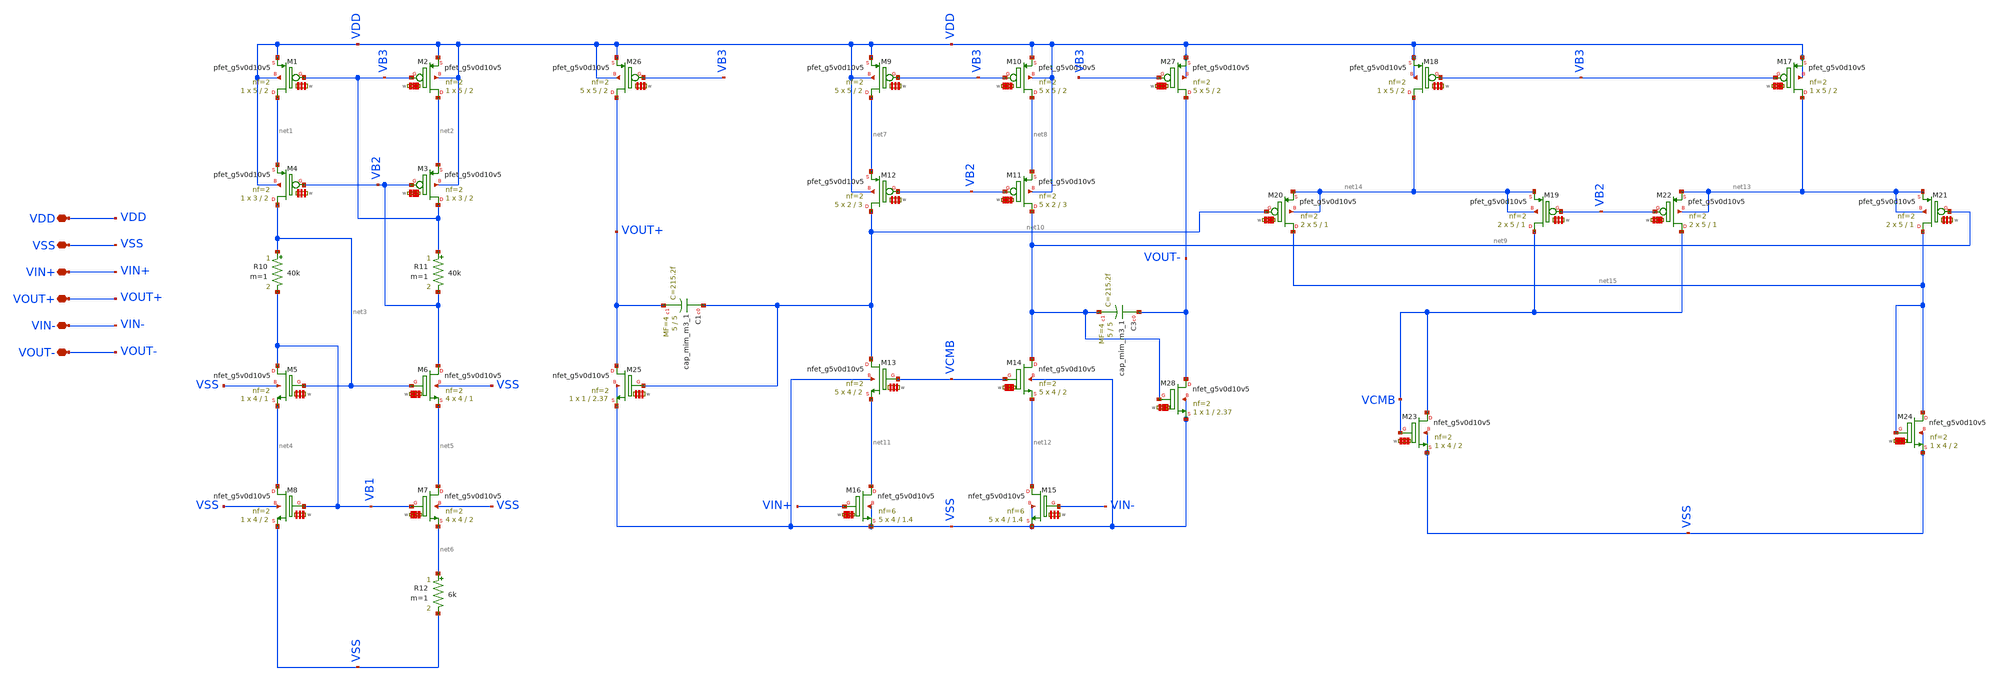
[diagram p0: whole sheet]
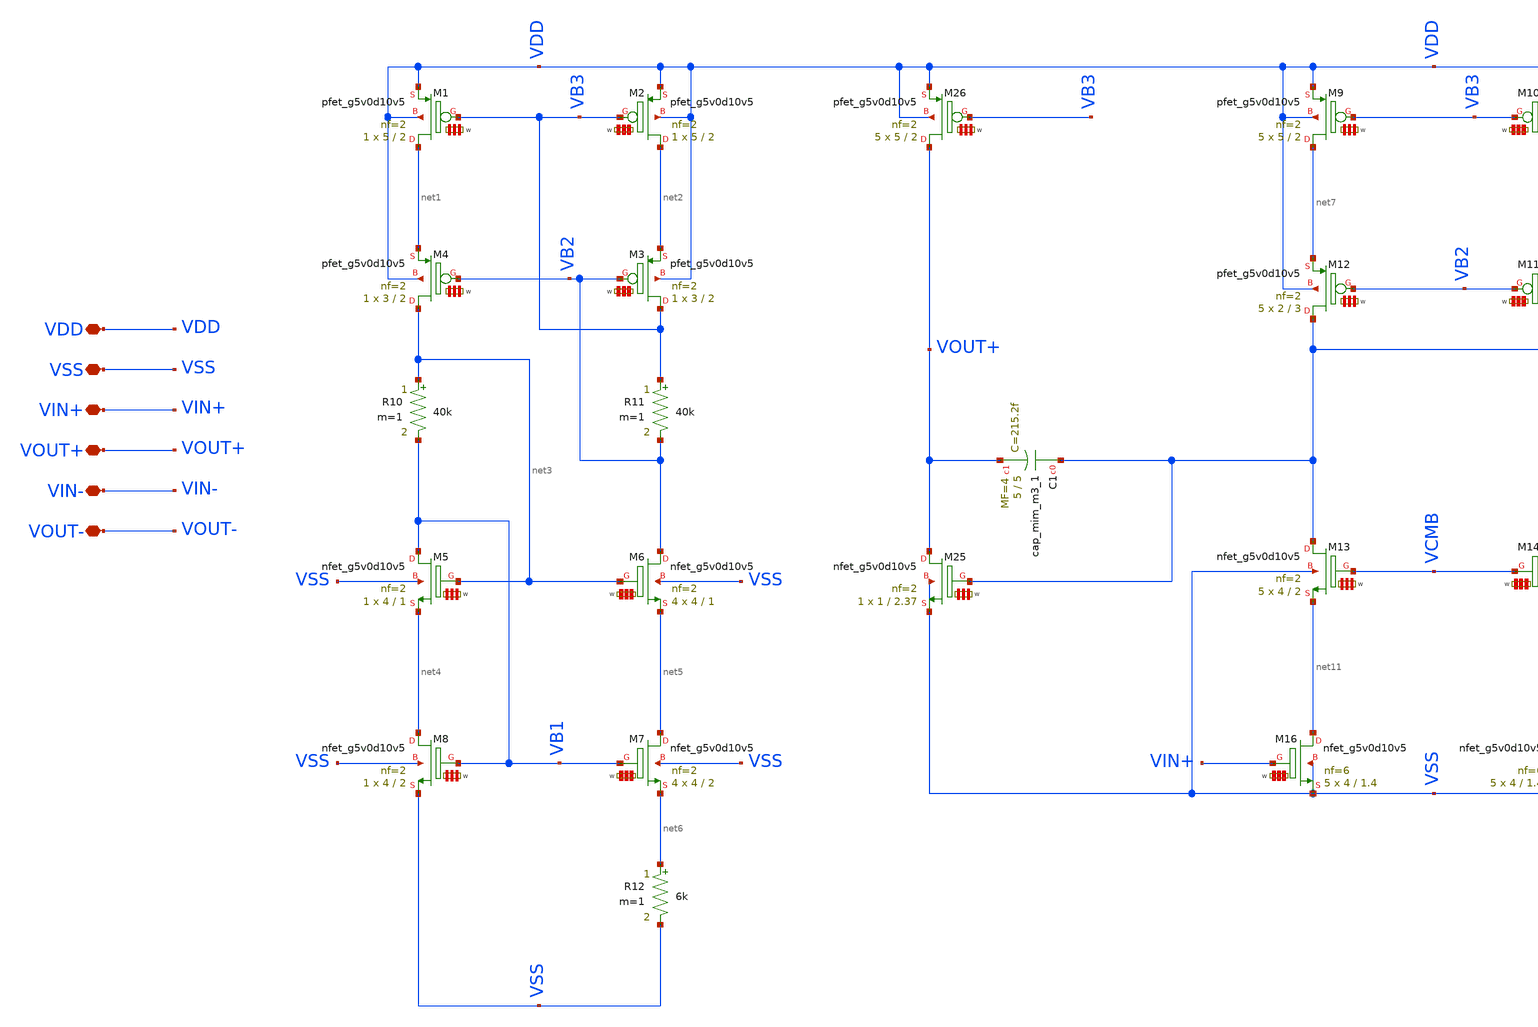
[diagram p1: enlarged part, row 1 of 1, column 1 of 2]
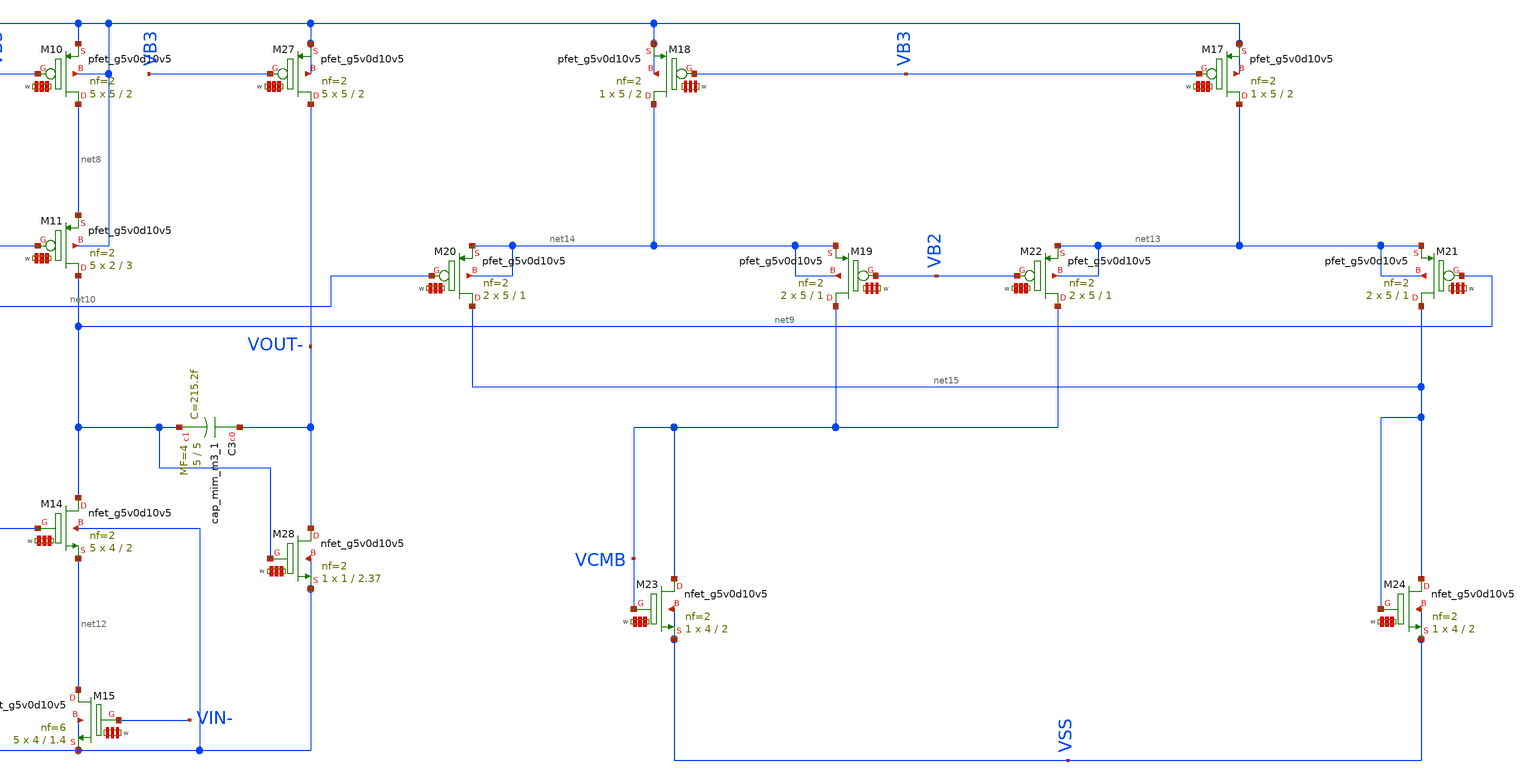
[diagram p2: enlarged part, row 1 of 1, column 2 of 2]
** sch_path: my_ip/sky130A/fully_differential_telescopic_cascode_5V_V1/fd_opamp.sch
**.subckt fd_opamp VDD VSS VIN+ VOUT+ VIN- VOUT-
*.iopin VDD
*.iopin VSS
*.iopin VIN+
*.iopin VOUT+
*.iopin VIN-
*.iopin VOUT-
XM1 net1 VB3 VDD VDD sky130_fd_pr__pfet_g5v0d10v5 L=2 W='5 * 2 ' nf=2 ad='int((2 + 1)/2) * 5 * 0.29'
+ as='int((2 + 2)/2) * 5 * 0.29' pd='2*int((2 + 1)/2) * (5 + 0.29)' ps='2*int((2 + 2)/2) * (5 + 0.29)'
+ nrd='0.29 / 5 / 2 ' nrs='0.29 / 5 / 2 ' sa=0 sb=0 sd=0 mult=1 m=1
XM3 VB3 VB2 net2 VDD sky130_fd_pr__pfet_g5v0d10v5 L=2 W='3 * 2 ' nf=2 ad='int((2 + 1)/2) * 3 * 0.29'
+ as='int((2 + 2)/2) * 3 * 0.29' pd='2*int((2 + 1)/2) * (3 + 0.29)' ps='2*int((2 + 2)/2) * (3 + 0.29)'
+ nrd='0.29 / 3 / 2 ' nrs='0.29 / 3 / 2 ' sa=0 sb=0 sd=0 mult=1 m=1
R10 net3 VB1 40k m=1
R11 VB3 VB2 40k m=1
XM7 net5 VB1 net6 VSS sky130_fd_pr__nfet_g5v0d10v5 L=2 W='4 * 2 ' nf=2 ad='int((nf+1)/2) * W / nf * 0.29'
+ as='int((nf+2)/2) * W / nf * 0.29' pd='2*int((nf+1)/2) * (W / nf + 0.29)' ps='2*int((nf+2)/2) * (W / nf + 0.29)'
+ nrd='0.29 / W ' nrs='0.29 / W ' sa=0 sb=0 sd=0 mult=4 m=4
R12 net6 VSS 6k m=1
XM2 net2 VB3 VDD VDD sky130_fd_pr__pfet_g5v0d10v5 L=2 W='5 * 2 ' nf=2 ad='int((2 + 1)/2) * 5 * 0.29'
+ as='int((2 + 2)/2) * 5 * 0.29' pd='2*int((2 + 1)/2) * (5 + 0.29)' ps='2*int((2 + 2)/2) * (5 + 0.29)'
+ nrd='0.29 / 5 / 2 ' nrs='0.29 / 5 / 2 ' sa=0 sb=0 sd=0 mult=1 m=1
XM6 VB2 net3 net5 VSS sky130_fd_pr__nfet_g5v0d10v5 L=1 W='4 * 2 ' nf=2 ad='int((nf+1)/2) * W / nf * 0.29'
+ as='int((nf+2)/2) * W / nf * 0.29' pd='2*int((nf+1)/2) * (W / nf + 0.29)' ps='2*int((nf+2)/2) * (W / nf + 0.29)'
+ nrd='0.29 / W ' nrs='0.29 / W ' sa=0 sb=0 sd=0 mult=4 m=4
XM5 VB1 net3 net4 VSS sky130_fd_pr__nfet_g5v0d10v5 L=1 W='4 * 2 ' nf=2 ad='int((nf+1)/2) * W / nf * 0.29'
+ as='int((nf+2)/2) * W / nf * 0.29' pd='2*int((nf+1)/2) * (W / nf + 0.29)' ps='2*int((nf+2)/2) * (W / nf + 0.29)'
+ nrd='0.29 / W ' nrs='0.29 / W ' sa=0 sb=0 sd=0 mult=1 m=1
XM8 net4 VB1 VSS VSS sky130_fd_pr__nfet_g5v0d10v5 L=2 W='4 * 2 ' nf=2 ad='int((nf+1)/2) * W / nf * 0.29'
+ as='int((nf+2)/2) * W / nf * 0.29' pd='2*int((nf+1)/2) * (W / nf + 0.29)' ps='2*int((nf+2)/2) * (W / nf + 0.29)'
+ nrd='0.29 / W ' nrs='0.29 / W ' sa=0 sb=0 sd=0 mult=1 m=1
XM4 net3 VB2 net1 VDD sky130_fd_pr__pfet_g5v0d10v5 L=2 W='3 * 2 ' nf=2 ad='int((2 + 1)/2) * 3 * 0.29'
+ as='int((2 + 2)/2) * 3 * 0.29' pd='2*int((2 + 1)/2) * (3 + 0.29)' ps='2*int((2 + 2)/2) * (3 + 0.29)'
+ nrd='0.29 / 3 / 2 ' nrs='0.29 / 3 / 2 ' sa=0 sb=0 sd=0 mult=1 m=1
XM11 net9 VB2 net8 VDD sky130_fd_pr__pfet_g5v0d10v5 L=3 W='2 * 2 ' nf=2 ad='int((2 + 1)/2) * 2 * 0.29'
+ as='int((2 + 2)/2) * 2 * 0.29' pd='2*int((2 + 1)/2) * (2 + 0.29)' ps='2*int((2 + 2)/2) * (2 + 0.29)'
+ nrd='0.29 / 2 / 2 ' nrs='0.29 / 2 / 2 ' sa=0 sb=0 sd=0 mult=5 m=5
XM12 net10 VB2 net7 VDD sky130_fd_pr__pfet_g5v0d10v5 L=3 W='2 * 2 ' nf=2 ad='int((2 + 1)/2) * 2 * 0.29'
+ as='int((2 + 2)/2) * 2 * 0.29' pd='2*int((2 + 1)/2) * (2 + 0.29)' ps='2*int((2 + 2)/2) * (2 + 0.29)'
+ nrd='0.29 / 2 / 2 ' nrs='0.29 / 2 / 2 ' sa=0 sb=0 sd=0 mult=5 m=5
XM15 net12 VIN- VSS VSS sky130_fd_pr__nfet_g5v0d10v5 L=1.4 W='4 * 6 ' nf=6 ad='int((nf+1)/2) * W / nf * 0.29'
+ as='int((nf+2)/2) * W / nf * 0.29' pd='2*int((nf+1)/2) * (W / nf + 0.29)' ps='2*int((nf+2)/2) * (W / nf + 0.29)'
+ nrd='0.29 / W ' nrs='0.29 / W ' sa=0 sb=0 sd=0 mult=5 m=5
XM19 VCMB VB2 net14 net14 sky130_fd_pr__pfet_g5v0d10v5 L=1 W='5 * 2 ' nf=2 ad='int((2 + 1)/2) * 5 * 0.29'
+ as='int((2 + 2)/2) * 5 * 0.29' pd='2*int((2 + 1)/2) * (5 + 0.29)' ps='2*int((2 + 2)/2) * (5 + 0.29)'
+ nrd='0.29 / 5 / 2 ' nrs='0.29 / 5 / 2 ' sa=0 sb=0 sd=0 mult=2 m=2
XM20 net15 net10 net14 net14 sky130_fd_pr__pfet_g5v0d10v5 L=1 W='5 * 2 ' nf=2 ad='int((2 + 1)/2) * 5 * 0.29'
+ as='int((2 + 2)/2) * 5 * 0.29' pd='2*int((2 + 1)/2) * (5 + 0.29)' ps='2*int((2 + 2)/2) * (5 + 0.29)'
+ nrd='0.29 / 5 / 2 ' nrs='0.29 / 5 / 2 ' sa=0 sb=0 sd=0 mult=2 m=2
XM21 net15 net9 net13 net13 sky130_fd_pr__pfet_g5v0d10v5 L=1 W='5 * 2 ' nf=2 ad='int((2 + 1)/2) * 5 * 0.29'
+ as='int((2 + 2)/2) * 5 * 0.29' pd='2*int((2 + 1)/2) * (5 + 0.29)' ps='2*int((2 + 2)/2) * (5 + 0.29)'
+ nrd='0.29 / 5 / 2 ' nrs='0.29 / 5 / 2 ' sa=0 sb=0 sd=0 mult=2 m=2
XM22 VCMB VB2 net13 net13 sky130_fd_pr__pfet_g5v0d10v5 L=1 W='5 * 2 ' nf=2 ad='int((2 + 1)/2) * 5 * 0.29'
+ as='int((2 + 2)/2) * 5 * 0.29' pd='2*int((2 + 1)/2) * (5 + 0.29)' ps='2*int((2 + 2)/2) * (5 + 0.29)'
+ nrd='0.29 / 5 / 2 ' nrs='0.29 / 5 / 2 ' sa=0 sb=0 sd=0 mult=2 m=2
XM16 net11 VIN+ VSS VSS sky130_fd_pr__nfet_g5v0d10v5 L=1.4 W='4 * 6 ' nf=6 ad='int((nf+1)/2) * W / nf * 0.29'
+ as='int((nf+2)/2) * W / nf * 0.29' pd='2*int((nf+1)/2) * (W / nf + 0.29)' ps='2*int((nf+2)/2) * (W / nf + 0.29)'
+ nrd='0.29 / W ' nrs='0.29 / W ' sa=0 sb=0 sd=0 mult=5 m=5
XM13 net10 VCMB net11 VSS sky130_fd_pr__nfet_g5v0d10v5 L=2 W='4 * 2 ' nf=2 ad='int((nf+1)/2) * W / nf * 0.29'
+ as='int((nf+2)/2) * W / nf * 0.29' pd='2*int((nf+1)/2) * (W / nf + 0.29)' ps='2*int((nf+2)/2) * (W / nf + 0.29)'
+ nrd='0.29 / W ' nrs='0.29 / W ' sa=0 sb=0 sd=0 mult=5 m=5
XM14 net9 VCMB net12 VSS sky130_fd_pr__nfet_g5v0d10v5 L=2 W='4 * 2 ' nf=2 ad='int((nf+1)/2) * W / nf * 0.29'
+ as='int((nf+2)/2) * W / nf * 0.29' pd='2*int((nf+1)/2) * (W / nf + 0.29)' ps='2*int((nf+2)/2) * (W / nf + 0.29)'
+ nrd='0.29 / W ' nrs='0.29 / W ' sa=0 sb=0 sd=0 mult=5 m=5
XM23 VCMB VCMB VSS VSS sky130_fd_pr__nfet_g5v0d10v5 L=2 W='4 * 2 ' nf=2 ad='int((nf+1)/2) * W / nf * 0.29'
+ as='int((nf+2)/2) * W / nf * 0.29' pd='2*int((nf+1)/2) * (W / nf + 0.29)' ps='2*int((nf+2)/2) * (W / nf + 0.29)'
+ nrd='0.29 / W ' nrs='0.29 / W ' sa=0 sb=0 sd=0 mult=1 m=1
XM24 net15 net15 VSS VSS sky130_fd_pr__nfet_g5v0d10v5 L=2 W='4 * 2 ' nf=2 ad='int((nf+1)/2) * W / nf * 0.29'
+ as='int((nf+2)/2) * W / nf * 0.29' pd='2*int((nf+1)/2) * (W / nf + 0.29)' ps='2*int((nf+2)/2) * (W / nf + 0.29)'
+ nrd='0.29 / W ' nrs='0.29 / W ' sa=0 sb=0 sd=0 mult=1 m=1
XM25 VOUT+ net10 VSS VSS sky130_fd_pr__nfet_g5v0d10v5 L=2.37 W='1 * 2 ' nf=2 ad='int((nf+1)/2) * W / nf * 0.29'
+ as='int((nf+2)/2) * W / nf * 0.29' pd='2*int((nf+1)/2) * (W / nf + 0.29)' ps='2*int((nf+2)/2) * (W / nf + 0.29)'
+ nrd='0.29 / W ' nrs='0.29 / W ' sa=0 sb=0 sd=0 mult=1 m=1
XC1 net10 VOUT+ sky130_fd_pr__cap_mim_m3_1 W=5 L=5 MF=4 m=4
XM9 net7 VB3 VDD VDD sky130_fd_pr__pfet_g5v0d10v5 L=2 W='5 * 2 ' nf=2 ad='int((2 + 1)/2) * 5 * 0.29'
+ as='int((2 + 2)/2) * 5 * 0.29' pd='2*int((2 + 1)/2) * (5 + 0.29)' ps='2*int((2 + 2)/2) * (5 + 0.29)'
+ nrd='0.29 / 5 / 2 ' nrs='0.29 / 5 / 2 ' sa=0 sb=0 sd=0 mult=5 m=5
XM10 net8 VB3 VDD VDD sky130_fd_pr__pfet_g5v0d10v5 L=2 W='5 * 2 ' nf=2 ad='int((2 + 1)/2) * 5 * 0.29'
+ as='int((2 + 2)/2) * 5 * 0.29' pd='2*int((2 + 1)/2) * (5 + 0.29)' ps='2*int((2 + 2)/2) * (5 + 0.29)'
+ nrd='0.29 / 5 / 2 ' nrs='0.29 / 5 / 2 ' sa=0 sb=0 sd=0 mult=5 m=5
XM17 net13 VB3 VDD VDD sky130_fd_pr__pfet_g5v0d10v5 L=2 W='5 * 2 ' nf=2 ad='int((2 + 1)/2) * 5 * 0.29'
+ as='int((2 + 2)/2) * 5 * 0.29' pd='2*int((2 + 1)/2) * (5 + 0.29)' ps='2*int((2 + 2)/2) * (5 + 0.29)'
+ nrd='0.29 / 5 / 2 ' nrs='0.29 / 5 / 2 ' sa=0 sb=0 sd=0 mult=1 m=1
XM18 net14 VB3 VDD VDD sky130_fd_pr__pfet_g5v0d10v5 L=2 W='5 * 2 ' nf=2 ad='int((2 + 1)/2) * 5 * 0.29'
+ as='int((2 + 2)/2) * 5 * 0.29' pd='2*int((2 + 1)/2) * (5 + 0.29)' ps='2*int((2 + 2)/2) * (5 + 0.29)'
+ nrd='0.29 / 5 / 2 ' nrs='0.29 / 5 / 2 ' sa=0 sb=0 sd=0 mult=1 m=1
XM26 VOUT+ VB3 VDD VDD sky130_fd_pr__pfet_g5v0d10v5 L=2 W='5 * 2 ' nf=2 ad='int((2 + 1)/2) * 5 * 0.29'
+ as='int((2 + 2)/2) * 5 * 0.29' pd='2*int((2 + 1)/2) * (5 + 0.29)' ps='2*int((2 + 2)/2) * (5 + 0.29)'
+ nrd='0.29 / 5 / 2 ' nrs='0.29 / 5 / 2 ' sa=0 sb=0 sd=0 mult=5 m=5
XC3 VOUT- net9 sky130_fd_pr__cap_mim_m3_1 W=5 L=5 MF=4 m=4
XM27 VOUT- VB3 VDD VDD sky130_fd_pr__pfet_g5v0d10v5 L=2 W='5 * 2 ' nf=2 ad='int((2 + 1)/2) * 5 * 0.29'
+ as='int((2 + 2)/2) * 5 * 0.29' pd='2*int((2 + 1)/2) * (5 + 0.29)' ps='2*int((2 + 2)/2) * (5 + 0.29)'
+ nrd='0.29 / 5 / 2 ' nrs='0.29 / 5 / 2 ' sa=0 sb=0 sd=0 mult=5 m=5
XM28 VOUT- net9 VSS VSS sky130_fd_pr__nfet_g5v0d10v5 L=2.37 W='1 * 2 ' nf=2 ad='int((nf+1)/2) * W / nf * 0.29'
+ as='int((nf+2)/2) * W / nf * 0.29' pd='2*int((nf+1)/2) * (W / nf + 0.29)' ps='2*int((nf+2)/2) * (W / nf + 0.29)'
+ nrd='0.29 / W ' nrs='0.29 / W ' sa=0 sb=0 sd=0 mult=1 m=1
**.ends
.end
